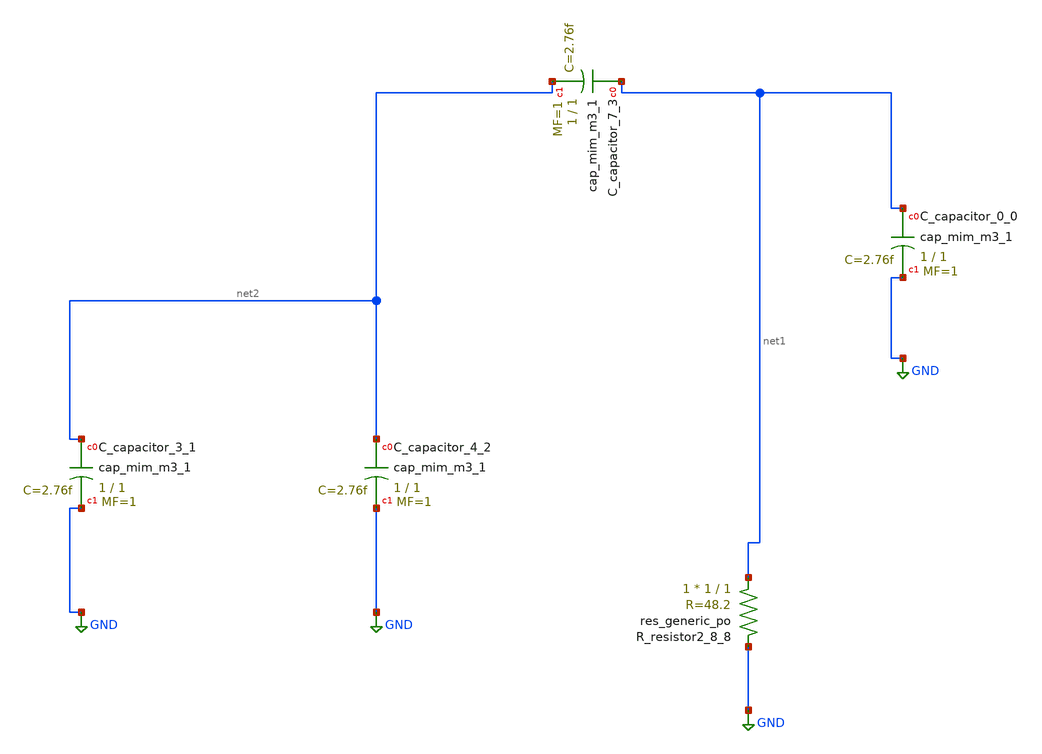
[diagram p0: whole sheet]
** sch_path: schematics/AMSNet/791.sch
**.subckt 791
XC_capacitor_0_0 net1 GND sky130_fd_pr__cap_mim_m3_1 W=1 L=1 MF=1 m=1
XC_capacitor_3_1 net2 GND sky130_fd_pr__cap_mim_m3_1 W=1 L=1 MF=1 m=1
XC_capacitor_4_2 net2 GND sky130_fd_pr__cap_mim_m3_1 W=1 L=1 MF=1 m=1
XC_capacitor_7_3 net1 net2 sky130_fd_pr__cap_mim_m3_1 W=1 L=1 MF=1 m=1
XR_resistor2_8_8 net1 GND sky130_fd_pr__res_generic_po W=1 L=1 m=1
**.ends
.GLOBAL GND
.end
